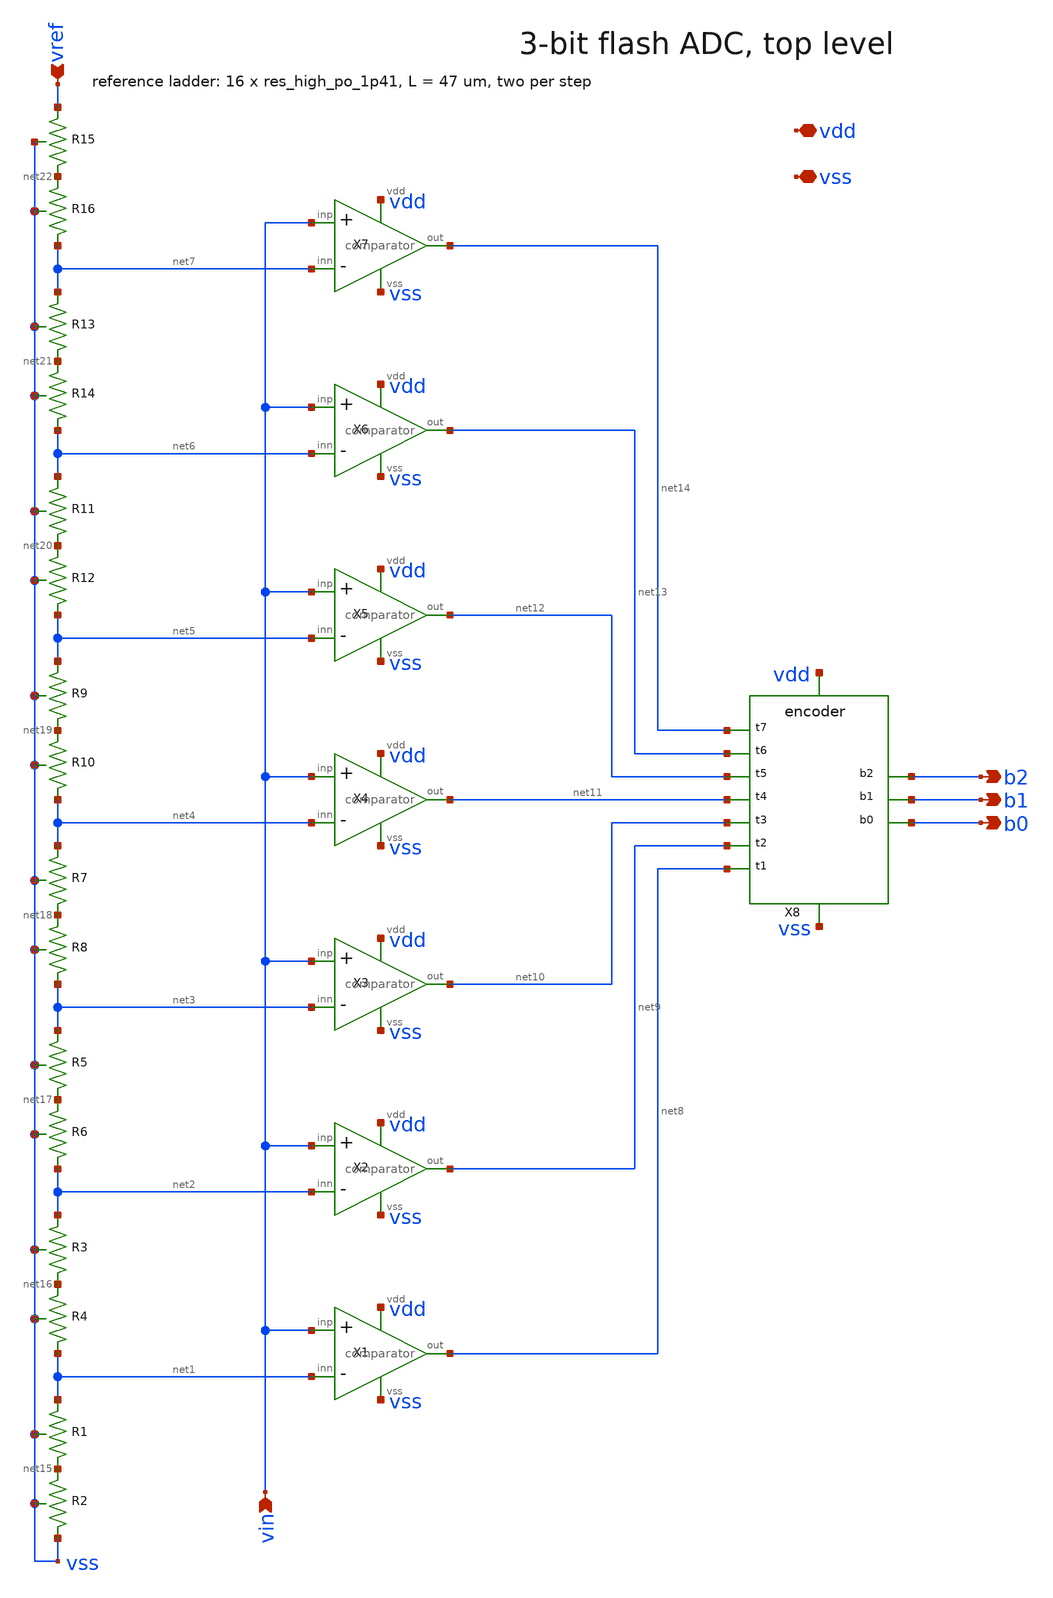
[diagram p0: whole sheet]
** sch_path: xschem/adc.sch
* SPDX-License-Identifier: Apache-2.0
* Copyright 2026 Mauro Rodriguez Blasco
**.subckt adc vin vref b2 b1 b0 vdd vss
*.ipin vin
*.ipin vref
*.opin b2
*.opin b1
*.opin b0
*.iopin vdd
*.iopin vss
XR1 net1 net15 vss sky130_fd_pr__res_high_po_1p41 L=47 mult=1 m=1
XR2 net15 vss vss sky130_fd_pr__res_high_po_1p41 L=47 mult=1 m=1
XR3 net2 net16 vss sky130_fd_pr__res_high_po_1p41 L=47 mult=1 m=1
XR4 net16 net1 vss sky130_fd_pr__res_high_po_1p41 L=47 mult=1 m=1
XR5 net3 net17 vss sky130_fd_pr__res_high_po_1p41 L=47 mult=1 m=1
XR6 net17 net2 vss sky130_fd_pr__res_high_po_1p41 L=47 mult=1 m=1
XR7 net4 net18 vss sky130_fd_pr__res_high_po_1p41 L=47 mult=1 m=1
XR8 net18 net3 vss sky130_fd_pr__res_high_po_1p41 L=47 mult=1 m=1
XR9 net5 net19 vss sky130_fd_pr__res_high_po_1p41 L=47 mult=1 m=1
XR10 net19 net4 vss sky130_fd_pr__res_high_po_1p41 L=47 mult=1 m=1
XR11 net6 net20 vss sky130_fd_pr__res_high_po_1p41 L=47 mult=1 m=1
XR12 net20 net5 vss sky130_fd_pr__res_high_po_1p41 L=47 mult=1 m=1
XR13 net7 net21 vss sky130_fd_pr__res_high_po_1p41 L=47 mult=1 m=1
XR14 net21 net6 vss sky130_fd_pr__res_high_po_1p41 L=47 mult=1 m=1
XR15 vref net22 vss sky130_fd_pr__res_high_po_1p41 L=47 mult=1 m=1
XR16 net22 net7 vss sky130_fd_pr__res_high_po_1p41 L=47 mult=1 m=1
X1 vin net1 net8 vdd vss comparator
X2 vin net2 net9 vdd vss comparator
X3 vin net3 net10 vdd vss comparator
X4 vin net4 net11 vdd vss comparator
X5 vin net5 net12 vdd vss comparator
X6 vin net6 net13 vdd vss comparator
X7 vin net7 net14 vdd vss comparator
X8 net8 net9 net10 net11 net12 net13 net14 b0 b1 b2 vdd vss encoder
**.ends
.end
